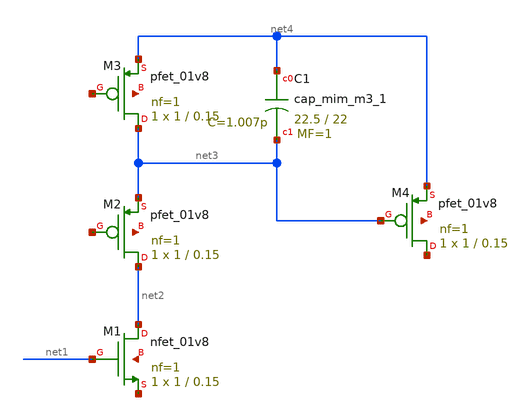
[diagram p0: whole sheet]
** sch_path: Neuron/ultralif/untitled.sch
**.subckt untitled
XM1 net2 net1 net5 net6 sky130_fd_pr__nfet_01v8 L=0.15 W=1 nf=1 ad='int((nf+1)/2) * W/nf * 0.29' as='int((nf+2)/2) * W/nf * 0.29'
+ pd='2*int((nf+1)/2) * (W/nf + 0.29)' ps='2*int((nf+2)/2) * (W/nf + 0.29)' nrd='0.29 / W' nrs='0.29 / W'
+ sa=0 sb=0 sd=0 mult=1 m=1
XM2 net2 net7 net3 net8 sky130_fd_pr__pfet_01v8 L=0.15 W=1 nf=1 ad='int((nf+1)/2) * W/nf * 0.29' as='int((nf+2)/2) * W/nf * 0.29'
+ pd='2*int((nf+1)/2) * (W/nf + 0.29)' ps='2*int((nf+2)/2) * (W/nf + 0.29)' nrd='0.29 / W' nrs='0.29 / W'
+ sa=0 sb=0 sd=0 mult=1 m=1
XM3 net3 net9 net4 net10 sky130_fd_pr__pfet_01v8 L=0.15 W=1 nf=1 ad='int((nf+1)/2) * W/nf * 0.29' as='int((nf+2)/2) * W/nf * 0.29'
+ pd='2*int((nf+1)/2) * (W/nf + 0.29)' ps='2*int((nf+2)/2) * (W/nf + 0.29)' nrd='0.29 / W' nrs='0.29 / W'
+ sa=0 sb=0 sd=0 mult=1 m=1
XM4 net11 net3 net4 net12 sky130_fd_pr__pfet_01v8 L=0.15 W=1 nf=1 ad='int((nf+1)/2) * W/nf * 0.29' as='int((nf+2)/2) * W/nf * 0.29'
+ pd='2*int((nf+1)/2) * (W/nf + 0.29)' ps='2*int((nf+2)/2) * (W/nf + 0.29)' nrd='0.29 / W' nrs='0.29 / W'
+ sa=0 sb=0 sd=0 mult=1 m=1
XC1 net4 net3 sky130_fd_pr__cap_mim_m3_1 W=22.5 L=22 MF=1 m=1
**.ends
.end
